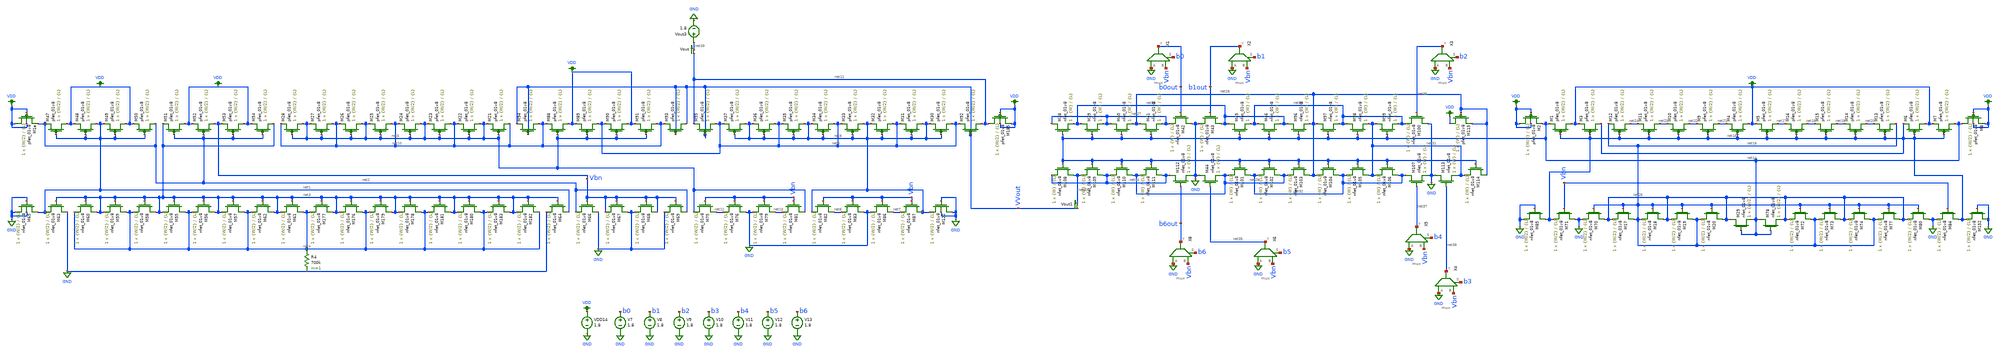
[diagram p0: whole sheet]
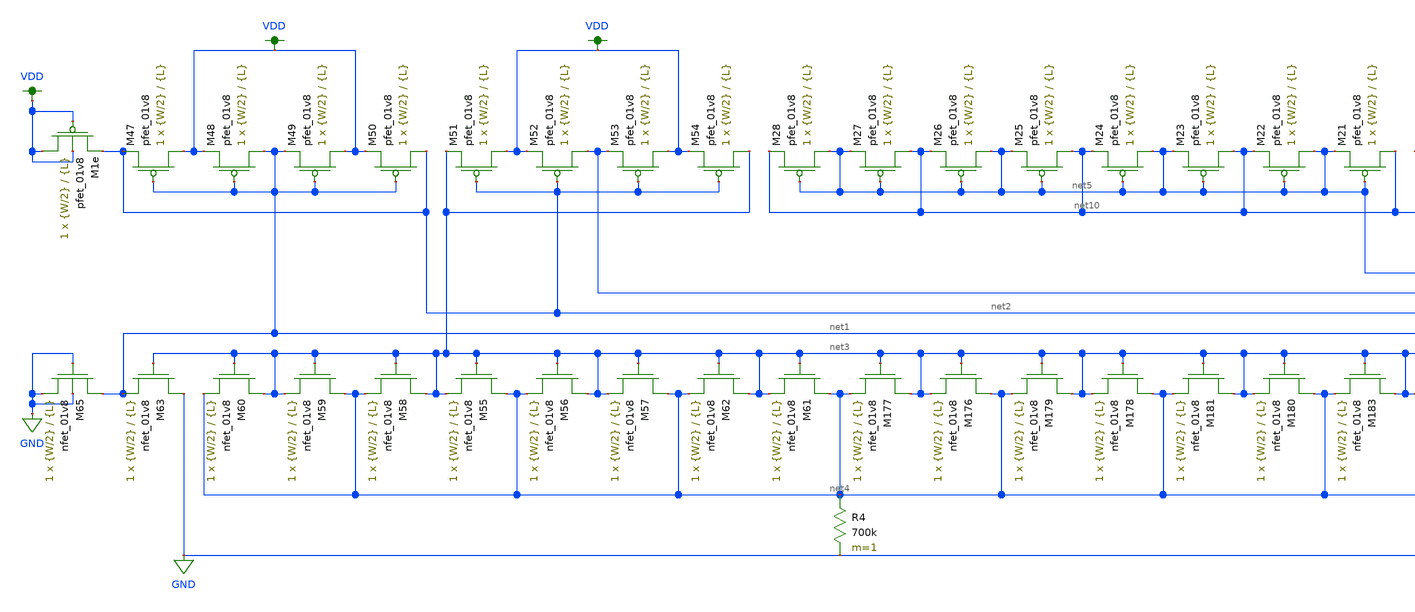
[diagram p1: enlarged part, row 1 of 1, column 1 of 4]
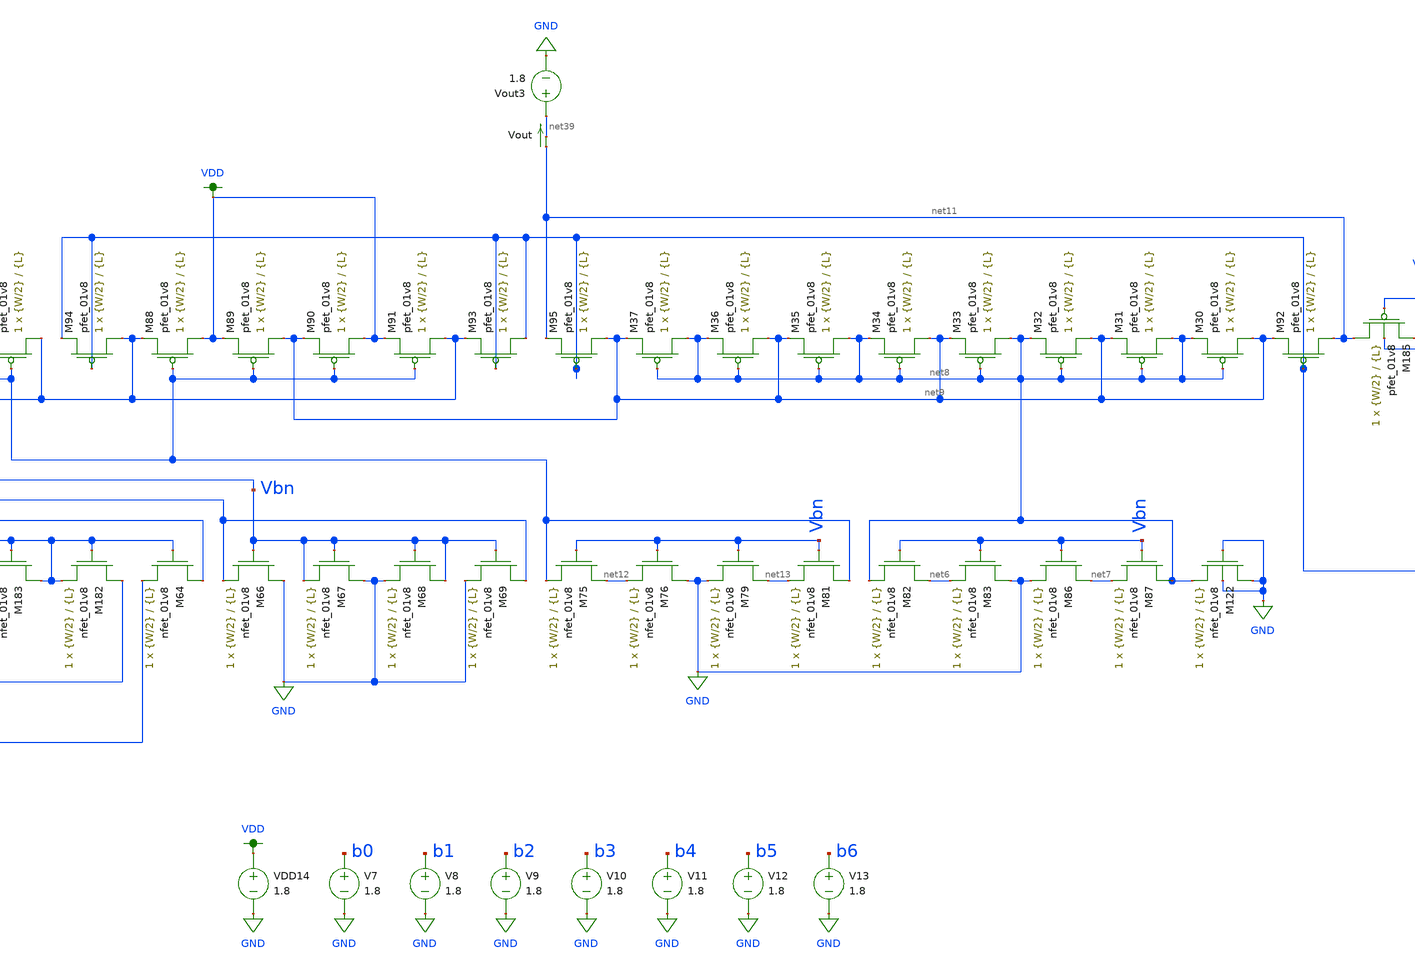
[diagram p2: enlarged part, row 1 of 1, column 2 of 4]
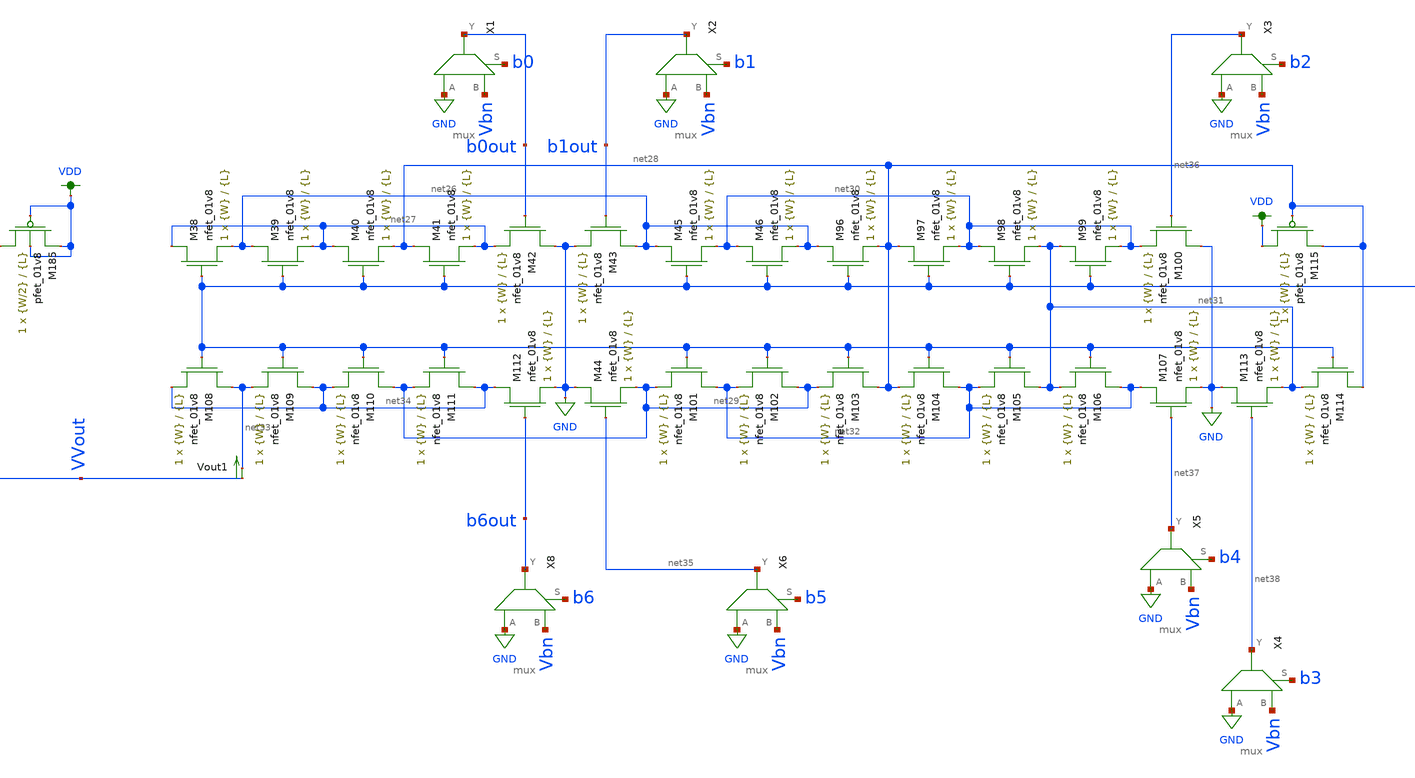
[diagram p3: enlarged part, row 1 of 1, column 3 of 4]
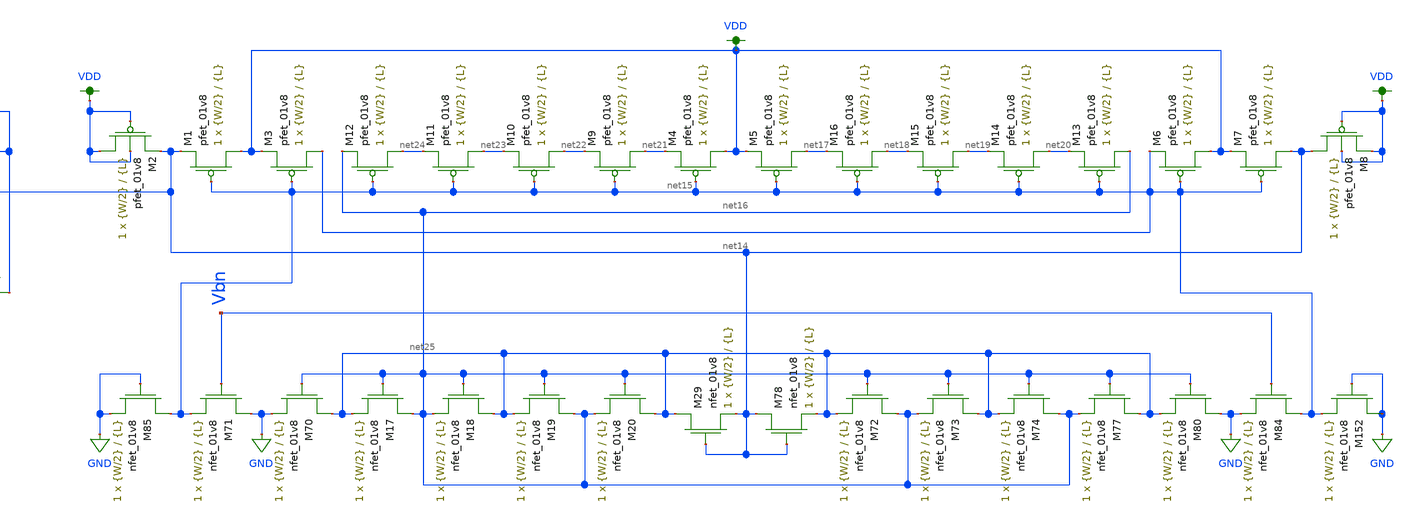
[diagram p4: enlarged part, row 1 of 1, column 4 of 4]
** sch_path: schematics/dac_voltage_current_current_mirror_lds.sch
**.subckt dac_voltage_current_current_mirror_lds
XM47 VDD net1 net2 VDD sky130_fd_pr__pfet_01v8 L={L} W={W/2} nf=1 ad='int((nf+1)/2) * W/nf * 0.29' as='int((nf+2)/2) * W/nf * 0.29'
+ pd='2*int((nf+1)/2) * (W/nf + 0.29)' ps='2*int((nf+2)/2) * (W/nf + 0.29)' nrd='0.29 / W' nrs='0.29 / W'
+ sa=0 sb=0 sd=0 mult=1 m=1
XM48 net1 net1 VDD VDD sky130_fd_pr__pfet_01v8 L={L} W={W/2} nf=1 ad='int((nf+1)/2) * W/nf * 0.29' as='int((nf+2)/2) * W/nf * 0.29'
+ pd='2*int((nf+1)/2) * (W/nf + 0.29)' ps='2*int((nf+2)/2) * (W/nf + 0.29)' nrd='0.29 / W' nrs='0.29 / W'
+ sa=0 sb=0 sd=0 mult=1 m=1
XM49 VDD net1 net1 VDD sky130_fd_pr__pfet_01v8 L={L} W={W/2} nf=1 ad='int((nf+1)/2) * W/nf * 0.29' as='int((nf+2)/2) * W/nf * 0.29'
+ pd='2*int((nf+1)/2) * (W/nf + 0.29)' ps='2*int((nf+2)/2) * (W/nf + 0.29)' nrd='0.29 / W' nrs='0.29 / W'
+ sa=0 sb=0 sd=0 mult=1 m=1
XM50 net2 net1 VDD VDD sky130_fd_pr__pfet_01v8 L={L} W={W/2} nf=1 ad='int((nf+1)/2) * W/nf * 0.29' as='int((nf+2)/2) * W/nf * 0.29'
+ pd='2*int((nf+1)/2) * (W/nf + 0.29)' ps='2*int((nf+2)/2) * (W/nf + 0.29)' nrd='0.29 / W' nrs='0.29 / W'
+ sa=0 sb=0 sd=0 mult=1 m=1
XM51 VDD net2 net3 VDD sky130_fd_pr__pfet_01v8 L={L} W={W/2} nf=1 ad='int((nf+1)/2) * W/nf * 0.29' as='int((nf+2)/2) * W/nf * 0.29'
+ pd='2*int((nf+1)/2) * (W/nf + 0.29)' ps='2*int((nf+2)/2) * (W/nf + 0.29)' nrd='0.29 / W' nrs='0.29 / W'
+ sa=0 sb=0 sd=0 mult=1 m=1
XM52 Vbn net2 VDD VDD sky130_fd_pr__pfet_01v8 L={L} W={W/2} nf=1 ad='int((nf+1)/2) * W/nf * 0.29' as='int((nf+2)/2) * W/nf * 0.29'
+ pd='2*int((nf+1)/2) * (W/nf + 0.29)' ps='2*int((nf+2)/2) * (W/nf + 0.29)' nrd='0.29 / W' nrs='0.29 / W'
+ sa=0 sb=0 sd=0 mult=1 m=1
XM53 VDD net2 Vbn VDD sky130_fd_pr__pfet_01v8 L={L} W={W/2} nf=1 ad='int((nf+1)/2) * W/nf * 0.29' as='int((nf+2)/2) * W/nf * 0.29'
+ pd='2*int((nf+1)/2) * (W/nf + 0.29)' ps='2*int((nf+2)/2) * (W/nf + 0.29)' nrd='0.29 / W' nrs='0.29 / W'
+ sa=0 sb=0 sd=0 mult=1 m=1
XM54 net3 net2 VDD VDD sky130_fd_pr__pfet_01v8 L={L} W={W/2} nf=1 ad='int((nf+1)/2) * W/nf * 0.29' as='int((nf+2)/2) * W/nf * 0.29'
+ pd='2*int((nf+1)/2) * (W/nf + 0.29)' ps='2*int((nf+2)/2) * (W/nf + 0.29)' nrd='0.29 / W' nrs='0.29 / W'
+ sa=0 sb=0 sd=0 mult=1 m=1
XM55 net4 net3 net3 GND sky130_fd_pr__nfet_01v8 L={L} W={W/2} nf=1 ad='int((nf+1)/2) * W/nf * 0.29' as='int((nf+2)/2) * W/nf * 0.29'
+ pd='2*int((nf+1)/2) * (W/nf + 0.29)' ps='2*int((nf+2)/2) * (W/nf + 0.29)' nrd='0.29 / W' nrs='0.29 / W'
+ sa=0 sb=0 sd=0 mult=1 m=1
XM56 net3 net3 net4 GND sky130_fd_pr__nfet_01v8 L={L} W={W/2} nf=1 ad='int((nf+1)/2) * W/nf * 0.29' as='int((nf+2)/2) * W/nf * 0.29'
+ pd='2*int((nf+1)/2) * (W/nf + 0.29)' ps='2*int((nf+2)/2) * (W/nf + 0.29)' nrd='0.29 / W' nrs='0.29 / W'
+ sa=0 sb=0 sd=0 mult=1 m=1
XM57 net4 net3 net3 GND sky130_fd_pr__nfet_01v8 L={L} W={W/2} nf=1 ad='int((nf+1)/2) * W/nf * 0.29' as='int((nf+2)/2) * W/nf * 0.29'
+ pd='2*int((nf+1)/2) * (W/nf + 0.29)' ps='2*int((nf+2)/2) * (W/nf + 0.29)' nrd='0.29 / W' nrs='0.29 / W'
+ sa=0 sb=0 sd=0 mult=1 m=1
XM58 net3 net3 net4 GND sky130_fd_pr__nfet_01v8 L={L} W={W/2} nf=1 ad='int((nf+1)/2) * W/nf * 0.29' as='int((nf+2)/2) * W/nf * 0.29'
+ pd='2*int((nf+1)/2) * (W/nf + 0.29)' ps='2*int((nf+2)/2) * (W/nf + 0.29)' nrd='0.29 / W' nrs='0.29 / W'
+ sa=0 sb=0 sd=0 mult=1 m=1
XM59 net4 net3 net3 GND sky130_fd_pr__nfet_01v8 L={L} W={W/2} nf=1 ad='int((nf+1)/2) * W/nf * 0.29' as='int((nf+2)/2) * W/nf * 0.29'
+ pd='2*int((nf+1)/2) * (W/nf + 0.29)' ps='2*int((nf+2)/2) * (W/nf + 0.29)' nrd='0.29 / W' nrs='0.29 / W'
+ sa=0 sb=0 sd=0 mult=1 m=1
XM60 net3 net3 net4 GND sky130_fd_pr__nfet_01v8 L={L} W={W/2} nf=1 ad='int((nf+1)/2) * W/nf * 0.29' as='int((nf+2)/2) * W/nf * 0.29'
+ pd='2*int((nf+1)/2) * (W/nf + 0.29)' ps='2*int((nf+2)/2) * (W/nf + 0.29)' nrd='0.29 / W' nrs='0.29 / W'
+ sa=0 sb=0 sd=0 mult=1 m=1
XM61 net4 net3 net3 GND sky130_fd_pr__nfet_01v8 L={L} W={W/2} nf=1 ad='int((nf+1)/2) * W/nf * 0.29' as='int((nf+2)/2) * W/nf * 0.29'
+ pd='2*int((nf+1)/2) * (W/nf + 0.29)' ps='2*int((nf+2)/2) * (W/nf + 0.29)' nrd='0.29 / W' nrs='0.29 / W'
+ sa=0 sb=0 sd=0 mult=1 m=1
XM62 net3 net3 net4 GND sky130_fd_pr__nfet_01v8 L={L} W={W/2} nf=1 ad='int((nf+1)/2) * W/nf * 0.29' as='int((nf+2)/2) * W/nf * 0.29'
+ pd='2*int((nf+1)/2) * (W/nf + 0.29)' ps='2*int((nf+2)/2) * (W/nf + 0.29)' nrd='0.29 / W' nrs='0.29 / W'
+ sa=0 sb=0 sd=0 mult=1 m=1
XM63 GND net3 net1 GND sky130_fd_pr__nfet_01v8 L={L} W={W/2} nf=1 ad='int((nf+1)/2) * W/nf * 0.29' as='int((nf+2)/2) * W/nf * 0.29'
+ pd='2*int((nf+1)/2) * (W/nf + 0.29)' ps='2*int((nf+2)/2) * (W/nf + 0.29)' nrd='0.29 / W' nrs='0.29 / W'
+ sa=0 sb=0 sd=0 mult=1 m=1
XM64 net1 net3 GND GND sky130_fd_pr__nfet_01v8 L={L} W={W/2} nf=1 ad='int((nf+1)/2) * W/nf * 0.29' as='int((nf+2)/2) * W/nf * 0.29'
+ pd='2*int((nf+1)/2) * (W/nf + 0.29)' ps='2*int((nf+2)/2) * (W/nf + 0.29)' nrd='0.29 / W' nrs='0.29 / W'
+ sa=0 sb=0 sd=0 mult=1 m=1
R4 net4 GND 700k m=1
XM1e VDD VDD net2 VDD sky130_fd_pr__pfet_01v8 L={L} W={W/2} nf=1 ad='int((nf+1)/2) * W/nf * 0.29' as='int((nf+2)/2) * W/nf * 0.29'
+ pd='2*int((nf+1)/2) * (W/nf + 0.29)' ps='2*int((nf+2)/2) * (W/nf + 0.29)' nrd='0.29 / W' nrs='0.29 / W'
+ sa=0 sb=0 sd=0 mult=1 m=1
XM65 net1 GND GND GND sky130_fd_pr__nfet_01v8 L={L} W={W/2} nf=1 ad='int((nf+1)/2) * W/nf * 0.29' as='int((nf+2)/2) * W/nf * 0.29'
+ pd='2*int((nf+1)/2) * (W/nf + 0.29)' ps='2*int((nf+2)/2) * (W/nf + 0.29)' nrd='0.29 / W' nrs='0.29 / W'
+ sa=0 sb=0 sd=0 mult=1 m=1
XM66 GND Vbn net2 GND sky130_fd_pr__nfet_01v8 L={L} W={W/2} nf=1 ad='int((nf+1)/2) * W/nf * 0.29' as='int((nf+2)/2) * W/nf * 0.29'
+ pd='2*int((nf+1)/2) * (W/nf + 0.29)' ps='2*int((nf+2)/2) * (W/nf + 0.29)' nrd='0.29 / W' nrs='0.29 / W'
+ sa=0 sb=0 sd=0 mult=1 m=1
XM67 GND Vbn Vbn GND sky130_fd_pr__nfet_01v8 L={L} W={W/2} nf=1 ad='int((nf+1)/2) * W/nf * 0.29' as='int((nf+2)/2) * W/nf * 0.29'
+ pd='2*int((nf+1)/2) * (W/nf + 0.29)' ps='2*int((nf+2)/2) * (W/nf + 0.29)' nrd='0.29 / W' nrs='0.29 / W'
+ sa=0 sb=0 sd=0 mult=1 m=1
XM68 Vbn Vbn GND GND sky130_fd_pr__nfet_01v8 L={L} W={W/2} nf=1 ad='int((nf+1)/2) * W/nf * 0.29' as='int((nf+2)/2) * W/nf * 0.29'
+ pd='2*int((nf+1)/2) * (W/nf + 0.29)' ps='2*int((nf+2)/2) * (W/nf + 0.29)' nrd='0.29 / W' nrs='0.29 / W'
+ sa=0 sb=0 sd=0 mult=1 m=1
XM69 net2 Vbn GND GND sky130_fd_pr__nfet_01v8 L={L} W={W/2} nf=1 ad='int((nf+1)/2) * W/nf * 0.29' as='int((nf+2)/2) * W/nf * 0.29'
+ pd='2*int((nf+1)/2) * (W/nf + 0.29)' ps='2*int((nf+2)/2) * (W/nf + 0.29)' nrd='0.29 / W' nrs='0.29 / W'
+ sa=0 sb=0 sd=0 mult=1 m=1
XM75 net12 Vbn net5 GND sky130_fd_pr__nfet_01v8 L={L} W={W/2} nf=1 ad='int((nf+1)/2) * W/nf * 0.29' as='int((nf+2)/2) * W/nf * 0.29'
+ pd='2*int((nf+1)/2) * (W/nf + 0.29)' ps='2*int((nf+2)/2) * (W/nf + 0.29)' nrd='0.29 / W' nrs='0.29 / W'
+ sa=0 sb=0 sd=0 mult=1 m=1
XM76 GND Vbn net12 GND sky130_fd_pr__nfet_01v8 L={L} W={W/2} nf=1 ad='int((nf+1)/2) * W/nf * 0.29' as='int((nf+2)/2) * W/nf * 0.29'
+ pd='2*int((nf+1)/2) * (W/nf + 0.29)' ps='2*int((nf+2)/2) * (W/nf + 0.29)' nrd='0.29 / W' nrs='0.29 / W'
+ sa=0 sb=0 sd=0 mult=1 m=1
XM79 net13 Vbn GND GND sky130_fd_pr__nfet_01v8 L={L} W={W/2} nf=1 ad='int((nf+1)/2) * W/nf * 0.29' as='int((nf+2)/2) * W/nf * 0.29'
+ pd='2*int((nf+1)/2) * (W/nf + 0.29)' ps='2*int((nf+2)/2) * (W/nf + 0.29)' nrd='0.29 / W' nrs='0.29 / W'
+ sa=0 sb=0 sd=0 mult=1 m=1
XM81 net5 Vbn net13 GND sky130_fd_pr__nfet_01v8 L={L} W={W/2} nf=1 ad='int((nf+1)/2) * W/nf * 0.29' as='int((nf+2)/2) * W/nf * 0.29'
+ pd='2*int((nf+1)/2) * (W/nf + 0.29)' ps='2*int((nf+2)/2) * (W/nf + 0.29)' nrd='0.29 / W' nrs='0.29 / W'
+ sa=0 sb=0 sd=0 mult=1 m=1
XM82 net6 Vbn net8 GND sky130_fd_pr__nfet_01v8 L={L} W={W/2} nf=1 ad='int((nf+1)/2) * W/nf * 0.29' as='int((nf+2)/2) * W/nf * 0.29'
+ pd='2*int((nf+1)/2) * (W/nf + 0.29)' ps='2*int((nf+2)/2) * (W/nf + 0.29)' nrd='0.29 / W' nrs='0.29 / W'
+ sa=0 sb=0 sd=0 mult=1 m=1
XM83 GND Vbn net6 GND sky130_fd_pr__nfet_01v8 L={L} W={W/2} nf=1 ad='int((nf+1)/2) * W/nf * 0.29' as='int((nf+2)/2) * W/nf * 0.29'
+ pd='2*int((nf+1)/2) * (W/nf + 0.29)' ps='2*int((nf+2)/2) * (W/nf + 0.29)' nrd='0.29 / W' nrs='0.29 / W'
+ sa=0 sb=0 sd=0 mult=1 m=1
XM86 net7 Vbn GND GND sky130_fd_pr__nfet_01v8 L={L} W={W/2} nf=1 ad='int((nf+1)/2) * W/nf * 0.29' as='int((nf+2)/2) * W/nf * 0.29'
+ pd='2*int((nf+1)/2) * (W/nf + 0.29)' ps='2*int((nf+2)/2) * (W/nf + 0.29)' nrd='0.29 / W' nrs='0.29 / W'
+ sa=0 sb=0 sd=0 mult=1 m=1
XM87 net8 Vbn net7 GND sky130_fd_pr__nfet_01v8 L={L} W={W/2} nf=1 ad='int((nf+1)/2) * W/nf * 0.29' as='int((nf+2)/2) * W/nf * 0.29'
+ pd='2*int((nf+1)/2) * (W/nf + 0.29)' ps='2*int((nf+2)/2) * (W/nf + 0.29)' nrd='0.29 / W' nrs='0.29 / W'
+ sa=0 sb=0 sd=0 mult=1 m=1
XM88 VDD net5 net10 VDD sky130_fd_pr__pfet_01v8 L={L} W={W/2} nf=1 ad='int((nf+1)/2) * W/nf * 0.29' as='int((nf+2)/2) * W/nf * 0.29'
+ pd='2*int((nf+1)/2) * (W/nf + 0.29)' ps='2*int((nf+2)/2) * (W/nf + 0.29)' nrd='0.29 / W' nrs='0.29 / W'
+ sa=0 sb=0 sd=0 mult=1 m=1
XM89 net9 net5 VDD VDD sky130_fd_pr__pfet_01v8 L={L} W={W/2} nf=1 ad='int((nf+1)/2) * W/nf * 0.29' as='int((nf+2)/2) * W/nf * 0.29'
+ pd='2*int((nf+1)/2) * (W/nf + 0.29)' ps='2*int((nf+2)/2) * (W/nf + 0.29)' nrd='0.29 / W' nrs='0.29 / W'
+ sa=0 sb=0 sd=0 mult=1 m=1
XM90 VDD net5 net9 VDD sky130_fd_pr__pfet_01v8 L={L} W={W/2} nf=1 ad='int((nf+1)/2) * W/nf * 0.29' as='int((nf+2)/2) * W/nf * 0.29'
+ pd='2*int((nf+1)/2) * (W/nf + 0.29)' ps='2*int((nf+2)/2) * (W/nf + 0.29)' nrd='0.29 / W' nrs='0.29 / W'
+ sa=0 sb=0 sd=0 mult=1 m=1
XM91 net10 net5 VDD VDD sky130_fd_pr__pfet_01v8 L={L} W={W/2} nf=1 ad='int((nf+1)/2) * W/nf * 0.29' as='int((nf+2)/2) * W/nf * 0.29'
+ pd='2*int((nf+1)/2) * (W/nf + 0.29)' ps='2*int((nf+2)/2) * (W/nf + 0.29)' nrd='0.29 / W' nrs='0.29 / W'
+ sa=0 sb=0 sd=0 mult=1 m=1
XM92 net11 VVout net9 VDD sky130_fd_pr__pfet_01v8 L={L} W={W/2} nf=1 ad='int((nf+1)/2) * W/nf * 0.29'
+ as='int((nf+2)/2) * W/nf * 0.29' pd='2*int((nf+1)/2) * (W/nf + 0.29)' ps='2*int((nf+2)/2) * (W/nf + 0.29)'
+ nrd='0.29 / W' nrs='0.29 / W' sa=0 sb=0 sd=0 mult=1 m=1
XM93 VVout VVout net10 VDD sky130_fd_pr__pfet_01v8 L={L} W={W/2} nf=1 ad='int((nf+1)/2) * W/nf * 0.29'
+ as='int((nf+2)/2) * W/nf * 0.29' pd='2*int((nf+1)/2) * (W/nf + 0.29)' ps='2*int((nf+2)/2) * (W/nf + 0.29)'
+ nrd='0.29 / W' nrs='0.29 / W' sa=0 sb=0 sd=0 mult=1 m=1
XM94 net10 VVout VVout VDD sky130_fd_pr__pfet_01v8 L={L} W={W/2} nf=1 ad='int((nf+1)/2) * W/nf * 0.29'
+ as='int((nf+2)/2) * W/nf * 0.29' pd='2*int((nf+1)/2) * (W/nf + 0.29)' ps='2*int((nf+2)/2) * (W/nf + 0.29)'
+ nrd='0.29 / W' nrs='0.29 / W' sa=0 sb=0 sd=0 mult=1 m=1
XM95 net9 VVout net11 VDD sky130_fd_pr__pfet_01v8 L={L} W={W/2} nf=1 ad='int((nf+1)/2) * W/nf * 0.29'
+ as='int((nf+2)/2) * W/nf * 0.29' pd='2*int((nf+1)/2) * (W/nf + 0.29)' ps='2*int((nf+2)/2) * (W/nf + 0.29)'
+ nrd='0.29 / W' nrs='0.29 / W' sa=0 sb=0 sd=0 mult=1 m=1
XM176 net4 net3 net3 GND sky130_fd_pr__nfet_01v8 L={L} W={W/2} nf=1 ad='int((nf+1)/2) * W/nf * 0.29'
+ as='int((nf+2)/2) * W/nf * 0.29' pd='2*int((nf+1)/2) * (W/nf + 0.29)' ps='2*int((nf+2)/2) * (W/nf + 0.29)'
+ nrd='0.29 / W' nrs='0.29 / W' sa=0 sb=0 sd=0 mult=1 m=1
XM177 net3 net3 net4 GND sky130_fd_pr__nfet_01v8 L={L} W={W/2} nf=1 ad='int((nf+1)/2) * W/nf * 0.29'
+ as='int((nf+2)/2) * W/nf * 0.29' pd='2*int((nf+1)/2) * (W/nf + 0.29)' ps='2*int((nf+2)/2) * (W/nf + 0.29)'
+ nrd='0.29 / W' nrs='0.29 / W' sa=0 sb=0 sd=0 mult=1 m=1
XM178 net4 net3 net3 GND sky130_fd_pr__nfet_01v8 L={L} W={W/2} nf=1 ad='int((nf+1)/2) * W/nf * 0.29'
+ as='int((nf+2)/2) * W/nf * 0.29' pd='2*int((nf+1)/2) * (W/nf + 0.29)' ps='2*int((nf+2)/2) * (W/nf + 0.29)'
+ nrd='0.29 / W' nrs='0.29 / W' sa=0 sb=0 sd=0 mult=1 m=1
XM179 net3 net3 net4 GND sky130_fd_pr__nfet_01v8 L={L} W={W/2} nf=1 ad='int((nf+1)/2) * W/nf * 0.29'
+ as='int((nf+2)/2) * W/nf * 0.29' pd='2*int((nf+1)/2) * (W/nf + 0.29)' ps='2*int((nf+2)/2) * (W/nf + 0.29)'
+ nrd='0.29 / W' nrs='0.29 / W' sa=0 sb=0 sd=0 mult=1 m=1
XM180 net4 net3 net3 GND sky130_fd_pr__nfet_01v8 L={L} W={W/2} nf=1 ad='int((nf+1)/2) * W/nf * 0.29'
+ as='int((nf+2)/2) * W/nf * 0.29' pd='2*int((nf+1)/2) * (W/nf + 0.29)' ps='2*int((nf+2)/2) * (W/nf + 0.29)'
+ nrd='0.29 / W' nrs='0.29 / W' sa=0 sb=0 sd=0 mult=1 m=1
XM181 net3 net3 net4 GND sky130_fd_pr__nfet_01v8 L={L} W={W/2} nf=1 ad='int((nf+1)/2) * W/nf * 0.29'
+ as='int((nf+2)/2) * W/nf * 0.29' pd='2*int((nf+1)/2) * (W/nf + 0.29)' ps='2*int((nf+2)/2) * (W/nf + 0.29)'
+ nrd='0.29 / W' nrs='0.29 / W' sa=0 sb=0 sd=0 mult=1 m=1
XM182 net4 net3 net3 GND sky130_fd_pr__nfet_01v8 L={L} W={W/2} nf=1 ad='int((nf+1)/2) * W/nf * 0.29'
+ as='int((nf+2)/2) * W/nf * 0.29' pd='2*int((nf+1)/2) * (W/nf + 0.29)' ps='2*int((nf+2)/2) * (W/nf + 0.29)'
+ nrd='0.29 / W' nrs='0.29 / W' sa=0 sb=0 sd=0 mult=1 m=1
XM183 net3 net3 net4 GND sky130_fd_pr__nfet_01v8 L={L} W={W/2} nf=1 ad='int((nf+1)/2) * W/nf * 0.29'
+ as='int((nf+2)/2) * W/nf * 0.29' pd='2*int((nf+1)/2) * (W/nf + 0.29)' ps='2*int((nf+2)/2) * (W/nf + 0.29)'
+ nrd='0.29 / W' nrs='0.29 / W' sa=0 sb=0 sd=0 mult=1 m=1
XM185 net11 VDD VDD VDD sky130_fd_pr__pfet_01v8 L={L} W={W/2} nf=1 ad='int((nf+1)/2) * W/nf * 0.29' as='int((nf+2)/2) * W/nf * 0.29'
+ pd='2*int((nf+1)/2) * (W/nf + 0.29)' ps='2*int((nf+2)/2) * (W/nf + 0.29)' nrd='0.29 / W' nrs='0.29 / W'
+ sa=0 sb=0 sd=0 mult=1 m=1
Vout net11 net39 0
.save i(vout)
XM21 net10 net5 net5 VDD sky130_fd_pr__pfet_01v8 L={L} W={W/2} nf=1 ad='int((nf+1)/2) * W/nf * 0.29'
+ as='int((nf+2)/2) * W/nf * 0.29' pd='2*int((nf+1)/2) * (W/nf + 0.29)' ps='2*int((nf+2)/2) * (W/nf + 0.29)'
+ nrd='0.29 / W' nrs='0.29 / W' sa=0 sb=0 sd=0 mult=1 m=1
XM22 net5 net5 net10 VDD sky130_fd_pr__pfet_01v8 L={L} W={W/2} nf=1 ad='int((nf+1)/2) * W/nf * 0.29'
+ as='int((nf+2)/2) * W/nf * 0.29' pd='2*int((nf+1)/2) * (W/nf + 0.29)' ps='2*int((nf+2)/2) * (W/nf + 0.29)'
+ nrd='0.29 / W' nrs='0.29 / W' sa=0 sb=0 sd=0 mult=1 m=1
XM23 net10 net5 net5 VDD sky130_fd_pr__pfet_01v8 L={L} W={W/2} nf=1 ad='int((nf+1)/2) * W/nf * 0.29'
+ as='int((nf+2)/2) * W/nf * 0.29' pd='2*int((nf+1)/2) * (W/nf + 0.29)' ps='2*int((nf+2)/2) * (W/nf + 0.29)'
+ nrd='0.29 / W' nrs='0.29 / W' sa=0 sb=0 sd=0 mult=1 m=1
XM24 net5 net5 net10 VDD sky130_fd_pr__pfet_01v8 L={L} W={W/2} nf=1 ad='int((nf+1)/2) * W/nf * 0.29'
+ as='int((nf+2)/2) * W/nf * 0.29' pd='2*int((nf+1)/2) * (W/nf + 0.29)' ps='2*int((nf+2)/2) * (W/nf + 0.29)'
+ nrd='0.29 / W' nrs='0.29 / W' sa=0 sb=0 sd=0 mult=1 m=1
XM25 net10 net5 net5 VDD sky130_fd_pr__pfet_01v8 L={L} W={W/2} nf=1 ad='int((nf+1)/2) * W/nf * 0.29'
+ as='int((nf+2)/2) * W/nf * 0.29' pd='2*int((nf+1)/2) * (W/nf + 0.29)' ps='2*int((nf+2)/2) * (W/nf + 0.29)'
+ nrd='0.29 / W' nrs='0.29 / W' sa=0 sb=0 sd=0 mult=1 m=1
XM26 net5 net5 net10 VDD sky130_fd_pr__pfet_01v8 L={L} W={W/2} nf=1 ad='int((nf+1)/2) * W/nf * 0.29'
+ as='int((nf+2)/2) * W/nf * 0.29' pd='2*int((nf+1)/2) * (W/nf + 0.29)' ps='2*int((nf+2)/2) * (W/nf + 0.29)'
+ nrd='0.29 / W' nrs='0.29 / W' sa=0 sb=0 sd=0 mult=1 m=1
XM27 net10 net5 net5 VDD sky130_fd_pr__pfet_01v8 L={L} W={W/2} nf=1 ad='int((nf+1)/2) * W/nf * 0.29'
+ as='int((nf+2)/2) * W/nf * 0.29' pd='2*int((nf+1)/2) * (W/nf + 0.29)' ps='2*int((nf+2)/2) * (W/nf + 0.29)'
+ nrd='0.29 / W' nrs='0.29 / W' sa=0 sb=0 sd=0 mult=1 m=1
XM28 net5 net5 net10 VDD sky130_fd_pr__pfet_01v8 L={L} W={W/2} nf=1 ad='int((nf+1)/2) * W/nf * 0.29'
+ as='int((nf+2)/2) * W/nf * 0.29' pd='2*int((nf+1)/2) * (W/nf + 0.29)' ps='2*int((nf+2)/2) * (W/nf + 0.29)'
+ nrd='0.29 / W' nrs='0.29 / W' sa=0 sb=0 sd=0 mult=1 m=1
XM30 net9 net8 net8 VDD sky130_fd_pr__pfet_01v8 L={L} W={W/2} nf=1 ad='int((nf+1)/2) * W/nf * 0.29' as='int((nf+2)/2) * W/nf * 0.29'
+ pd='2*int((nf+1)/2) * (W/nf + 0.29)' ps='2*int((nf+2)/2) * (W/nf + 0.29)' nrd='0.29 / W' nrs='0.29 / W'
+ sa=0 sb=0 sd=0 mult=1 m=1
XM31 net8 net8 net9 VDD sky130_fd_pr__pfet_01v8 L={L} W={W/2} nf=1 ad='int((nf+1)/2) * W/nf * 0.29' as='int((nf+2)/2) * W/nf * 0.29'
+ pd='2*int((nf+1)/2) * (W/nf + 0.29)' ps='2*int((nf+2)/2) * (W/nf + 0.29)' nrd='0.29 / W' nrs='0.29 / W'
+ sa=0 sb=0 sd=0 mult=1 m=1
XM32 net9 net8 net8 VDD sky130_fd_pr__pfet_01v8 L={L} W={W/2} nf=1 ad='int((nf+1)/2) * W/nf * 0.29' as='int((nf+2)/2) * W/nf * 0.29'
+ pd='2*int((nf+1)/2) * (W/nf + 0.29)' ps='2*int((nf+2)/2) * (W/nf + 0.29)' nrd='0.29 / W' nrs='0.29 / W'
+ sa=0 sb=0 sd=0 mult=1 m=1
XM33 net8 net8 net9 VDD sky130_fd_pr__pfet_01v8 L={L} W={W/2} nf=1 ad='int((nf+1)/2) * W/nf * 0.29' as='int((nf+2)/2) * W/nf * 0.29'
+ pd='2*int((nf+1)/2) * (W/nf + 0.29)' ps='2*int((nf+2)/2) * (W/nf + 0.29)' nrd='0.29 / W' nrs='0.29 / W'
+ sa=0 sb=0 sd=0 mult=1 m=1
XM34 net9 net8 net8 VDD sky130_fd_pr__pfet_01v8 L={L} W={W/2} nf=1 ad='int((nf+1)/2) * W/nf * 0.29' as='int((nf+2)/2) * W/nf * 0.29'
+ pd='2*int((nf+1)/2) * (W/nf + 0.29)' ps='2*int((nf+2)/2) * (W/nf + 0.29)' nrd='0.29 / W' nrs='0.29 / W'
+ sa=0 sb=0 sd=0 mult=1 m=1
XM35 net8 net8 net9 VDD sky130_fd_pr__pfet_01v8 L={L} W={W/2} nf=1 ad='int((nf+1)/2) * W/nf * 0.29' as='int((nf+2)/2) * W/nf * 0.29'
+ pd='2*int((nf+1)/2) * (W/nf + 0.29)' ps='2*int((nf+2)/2) * (W/nf + 0.29)' nrd='0.29 / W' nrs='0.29 / W'
+ sa=0 sb=0 sd=0 mult=1 m=1
XM36 net9 net8 net8 VDD sky130_fd_pr__pfet_01v8 L={L} W={W/2} nf=1 ad='int((nf+1)/2) * W/nf * 0.29' as='int((nf+2)/2) * W/nf * 0.29'
+ pd='2*int((nf+1)/2) * (W/nf + 0.29)' ps='2*int((nf+2)/2) * (W/nf + 0.29)' nrd='0.29 / W' nrs='0.29 / W'
+ sa=0 sb=0 sd=0 mult=1 m=1
XM37 net8 net8 net9 VDD sky130_fd_pr__pfet_01v8 L={L} W={W/2} nf=1 ad='int((nf+1)/2) * W/nf * 0.29' as='int((nf+2)/2) * W/nf * 0.29'
+ pd='2*int((nf+1)/2) * (W/nf + 0.29)' ps='2*int((nf+2)/2) * (W/nf + 0.29)' nrd='0.29 / W' nrs='0.29 / W'
+ sa=0 sb=0 sd=0 mult=1 m=1
XM122 GND GND net8 GND sky130_fd_pr__nfet_01v8 L={L} W={W/2} nf=1 ad='int((nf+1)/2) * W/nf * 0.29' as='int((nf+2)/2) * W/nf * 0.29'
+ pd='2*int((nf+1)/2) * (W/nf + 0.29)' ps='2*int((nf+2)/2) * (W/nf + 0.29)' nrd='0.29 / W' nrs='0.29 / W'
+ sa=0 sb=0 sd=0 mult=1 m=1
XM1 VDD net15 net14 VDD sky130_fd_pr__pfet_01v8 L={L} W={W/2} nf=1 ad='int((nf+1)/2) * W/nf * 0.29' as='int((nf+2)/2) * W/nf * 0.29'
+ pd='2*int((nf+1)/2) * (W/nf + 0.29)' ps='2*int((nf+2)/2) * (W/nf + 0.29)' nrd='0.29 / W' nrs='0.29 / W'
+ sa=0 sb=0 sd=0 mult=1 m=1
XM2 VDD VDD net14 VDD sky130_fd_pr__pfet_01v8 L={L} W={W/2} nf=1 ad='int((nf+1)/2) * W/nf * 0.29' as='int((nf+2)/2) * W/nf * 0.29'
+ pd='2*int((nf+1)/2) * (W/nf + 0.29)' ps='2*int((nf+2)/2) * (W/nf + 0.29)' nrd='0.29 / W' nrs='0.29 / W'
+ sa=0 sb=0 sd=0 mult=1 m=1
XM3 net15 net15 VDD VDD sky130_fd_pr__pfet_01v8 L={L} W={W/2} nf=1 ad='int((nf+1)/2) * W/nf * 0.29' as='int((nf+2)/2) * W/nf * 0.29'
+ pd='2*int((nf+1)/2) * (W/nf + 0.29)' ps='2*int((nf+2)/2) * (W/nf + 0.29)' nrd='0.29 / W' nrs='0.29 / W'
+ sa=0 sb=0 sd=0 mult=1 m=1
XM4 VDD net15 net21 VDD sky130_fd_pr__pfet_01v8 L={L} W={W/2} nf=1 ad='int((nf+1)/2) * W/nf * 0.29' as='int((nf+2)/2) * W/nf * 0.29'
+ pd='2*int((nf+1)/2) * (W/nf + 0.29)' ps='2*int((nf+2)/2) * (W/nf + 0.29)' nrd='0.29 / W' nrs='0.29 / W'
+ sa=0 sb=0 sd=0 mult=1 m=1
XM5 net17 net15 VDD VDD sky130_fd_pr__pfet_01v8 L={L} W={W/2} nf=1 ad='int((nf+1)/2) * W/nf * 0.29' as='int((nf+2)/2) * W/nf * 0.29'
+ pd='2*int((nf+1)/2) * (W/nf + 0.29)' ps='2*int((nf+2)/2) * (W/nf + 0.29)' nrd='0.29 / W' nrs='0.29 / W'
+ sa=0 sb=0 sd=0 mult=1 m=1
XM6 VDD net15 net15 VDD sky130_fd_pr__pfet_01v8 L={L} W={W/2} nf=1 ad='int((nf+1)/2) * W/nf * 0.29' as='int((nf+2)/2) * W/nf * 0.29'
+ pd='2*int((nf+1)/2) * (W/nf + 0.29)' ps='2*int((nf+2)/2) * (W/nf + 0.29)' nrd='0.29 / W' nrs='0.29 / W'
+ sa=0 sb=0 sd=0 mult=1 m=1
XM7 net14 net15 VDD VDD sky130_fd_pr__pfet_01v8 L={L} W={W/2} nf=1 ad='int((nf+1)/2) * W/nf * 0.29' as='int((nf+2)/2) * W/nf * 0.29'
+ pd='2*int((nf+1)/2) * (W/nf + 0.29)' ps='2*int((nf+2)/2) * (W/nf + 0.29)' nrd='0.29 / W' nrs='0.29 / W'
+ sa=0 sb=0 sd=0 mult=1 m=1
XM8 net14 VDD VDD VDD sky130_fd_pr__pfet_01v8 L={L} W={W/2} nf=1 ad='int((nf+1)/2) * W/nf * 0.29' as='int((nf+2)/2) * W/nf * 0.29'
+ pd='2*int((nf+1)/2) * (W/nf + 0.29)' ps='2*int((nf+2)/2) * (W/nf + 0.29)' nrd='0.29 / W' nrs='0.29 / W'
+ sa=0 sb=0 sd=0 mult=1 m=1
XM9 net21 net15 net22 VDD sky130_fd_pr__pfet_01v8 L={L} W={W/2} nf=1 ad='int((nf+1)/2) * W/nf * 0.29'
+ as='int((nf+2)/2) * W/nf * 0.29' pd='2*int((nf+1)/2) * (W/nf + 0.29)' ps='2*int((nf+2)/2) * (W/nf + 0.29)'
+ nrd='0.29 / W' nrs='0.29 / W' sa=0 sb=0 sd=0 mult=1 m=1
XM10 net22 net15 net23 VDD sky130_fd_pr__pfet_01v8 L={L} W={W/2} nf=1 ad='int((nf+1)/2) * W/nf * 0.29'
+ as='int((nf+2)/2) * W/nf * 0.29' pd='2*int((nf+1)/2) * (W/nf + 0.29)' ps='2*int((nf+2)/2) * (W/nf + 0.29)'
+ nrd='0.29 / W' nrs='0.29 / W' sa=0 sb=0 sd=0 mult=1 m=1
XM11 net23 net15 net24 VDD sky130_fd_pr__pfet_01v8 L={L} W={W/2} nf=1 ad='int((nf+1)/2) * W/nf * 0.29'
+ as='int((nf+2)/2) * W/nf * 0.29' pd='2*int((nf+1)/2) * (W/nf + 0.29)' ps='2*int((nf+2)/2) * (W/nf + 0.29)'
+ nrd='0.29 / W' nrs='0.29 / W' sa=0 sb=0 sd=0 mult=1 m=1
XM12 net24 net15 net16 VDD sky130_fd_pr__pfet_01v8 L={L} W={W/2} nf=1 ad='int((nf+1)/2) * W/nf * 0.29'
+ as='int((nf+2)/2) * W/nf * 0.29' pd='2*int((nf+1)/2) * (W/nf + 0.29)' ps='2*int((nf+2)/2) * (W/nf + 0.29)'
+ nrd='0.29 / W' nrs='0.29 / W' sa=0 sb=0 sd=0 mult=1 m=1
XM13 net16 net15 net20 VDD sky130_fd_pr__pfet_01v8 L={L} W={W/2} nf=1 ad='int((nf+1)/2) * W/nf * 0.29'
+ as='int((nf+2)/2) * W/nf * 0.29' pd='2*int((nf+1)/2) * (W/nf + 0.29)' ps='2*int((nf+2)/2) * (W/nf + 0.29)'
+ nrd='0.29 / W' nrs='0.29 / W' sa=0 sb=0 sd=0 mult=1 m=1
XM14 net20 net15 net19 VDD sky130_fd_pr__pfet_01v8 L={L} W={W/2} nf=1 ad='int((nf+1)/2) * W/nf * 0.29'
+ as='int((nf+2)/2) * W/nf * 0.29' pd='2*int((nf+1)/2) * (W/nf + 0.29)' ps='2*int((nf+2)/2) * (W/nf + 0.29)'
+ nrd='0.29 / W' nrs='0.29 / W' sa=0 sb=0 sd=0 mult=1 m=1
XM15 net19 net15 net18 VDD sky130_fd_pr__pfet_01v8 L={L} W={W/2} nf=1 ad='int((nf+1)/2) * W/nf * 0.29'
+ as='int((nf+2)/2) * W/nf * 0.29' pd='2*int((nf+1)/2) * (W/nf + 0.29)' ps='2*int((nf+2)/2) * (W/nf + 0.29)'
+ nrd='0.29 / W' nrs='0.29 / W' sa=0 sb=0 sd=0 mult=1 m=1
XM16 net18 net15 net17 VDD sky130_fd_pr__pfet_01v8 L={L} W={W/2} nf=1 ad='int((nf+1)/2) * W/nf * 0.29'
+ as='int((nf+2)/2) * W/nf * 0.29' pd='2*int((nf+1)/2) * (W/nf + 0.29)' ps='2*int((nf+2)/2) * (W/nf + 0.29)'
+ nrd='0.29 / W' nrs='0.29 / W' sa=0 sb=0 sd=0 mult=1 m=1
XM17 net16 net16 net25 GND sky130_fd_pr__nfet_01v8 L={L} W={W/2} nf=1 ad='int((nf+1)/2) * W/nf * 0.29'
+ as='int((nf+2)/2) * W/nf * 0.29' pd='2*int((nf+1)/2) * (W/nf + 0.29)' ps='2*int((nf+2)/2) * (W/nf + 0.29)'
+ nrd='0.29 / W' nrs='0.29 / W' sa=0 sb=0 sd=0 mult=1 m=1
XM18 net25 net16 net16 GND sky130_fd_pr__nfet_01v8 L={L} W={W/2} nf=1 ad='int((nf+1)/2) * W/nf * 0.29'
+ as='int((nf+2)/2) * W/nf * 0.29' pd='2*int((nf+1)/2) * (W/nf + 0.29)' ps='2*int((nf+2)/2) * (W/nf + 0.29)'
+ nrd='0.29 / W' nrs='0.29 / W' sa=0 sb=0 sd=0 mult=1 m=1
XM19 net16 net16 net25 GND sky130_fd_pr__nfet_01v8 L={L} W={W/2} nf=1 ad='int((nf+1)/2) * W/nf * 0.29'
+ as='int((nf+2)/2) * W/nf * 0.29' pd='2*int((nf+1)/2) * (W/nf + 0.29)' ps='2*int((nf+2)/2) * (W/nf + 0.29)'
+ nrd='0.29 / W' nrs='0.29 / W' sa=0 sb=0 sd=0 mult=1 m=1
XM20 net25 net16 net16 GND sky130_fd_pr__nfet_01v8 L={L} W={W/2} nf=1 ad='int((nf+1)/2) * W/nf * 0.29'
+ as='int((nf+2)/2) * W/nf * 0.29' pd='2*int((nf+1)/2) * (W/nf + 0.29)' ps='2*int((nf+2)/2) * (W/nf + 0.29)'
+ nrd='0.29 / W' nrs='0.29 / W' sa=0 sb=0 sd=0 mult=1 m=1
XM29 net25 net14 net14 GND sky130_fd_pr__nfet_01v8 L={L} W={W/2} nf=1 ad='int((nf+1)/2) * W/nf * 0.29'
+ as='int((nf+2)/2) * W/nf * 0.29' pd='2*int((nf+1)/2) * (W/nf + 0.29)' ps='2*int((nf+2)/2) * (W/nf + 0.29)'
+ nrd='0.29 / W' nrs='0.29 / W' sa=0 sb=0 sd=0 mult=1 m=1
XM70 net25 net16 GND GND sky130_fd_pr__nfet_01v8 L={L} W={W/2} nf=1 ad='int((nf+1)/2) * W/nf * 0.29'
+ as='int((nf+2)/2) * W/nf * 0.29' pd='2*int((nf+1)/2) * (W/nf + 0.29)' ps='2*int((nf+2)/2) * (W/nf + 0.29)'
+ nrd='0.29 / W' nrs='0.29 / W' sa=0 sb=0 sd=0 mult=1 m=1
XM71 GND Vbn net15 GND sky130_fd_pr__nfet_01v8 L={L} W={W/2} nf=1 ad='int((nf+1)/2) * W/nf * 0.29' as='int((nf+2)/2) * W/nf * 0.29'
+ pd='2*int((nf+1)/2) * (W/nf + 0.29)' ps='2*int((nf+2)/2) * (W/nf + 0.29)' nrd='0.29 / W' nrs='0.29 / W'
+ sa=0 sb=0 sd=0 mult=1 m=1
XM72 net16 net16 net25 GND sky130_fd_pr__nfet_01v8 L={L} W={W/2} nf=1 ad='int((nf+1)/2) * W/nf * 0.29'
+ as='int((nf+2)/2) * W/nf * 0.29' pd='2*int((nf+1)/2) * (W/nf + 0.29)' ps='2*int((nf+2)/2) * (W/nf + 0.29)'
+ nrd='0.29 / W' nrs='0.29 / W' sa=0 sb=0 sd=0 mult=1 m=1
XM73 net25 net16 net16 GND sky130_fd_pr__nfet_01v8 L={L} W={W/2} nf=1 ad='int((nf+1)/2) * W/nf * 0.29'
+ as='int((nf+2)/2) * W/nf * 0.29' pd='2*int((nf+1)/2) * (W/nf + 0.29)' ps='2*int((nf+2)/2) * (W/nf + 0.29)'
+ nrd='0.29 / W' nrs='0.29 / W' sa=0 sb=0 sd=0 mult=1 m=1
XM74 net16 net16 net25 GND sky130_fd_pr__nfet_01v8 L={L} W={W/2} nf=1 ad='int((nf+1)/2) * W/nf * 0.29'
+ as='int((nf+2)/2) * W/nf * 0.29' pd='2*int((nf+1)/2) * (W/nf + 0.29)' ps='2*int((nf+2)/2) * (W/nf + 0.29)'
+ nrd='0.29 / W' nrs='0.29 / W' sa=0 sb=0 sd=0 mult=1 m=1
XM77 net25 net16 net16 GND sky130_fd_pr__nfet_01v8 L={L} W={W/2} nf=1 ad='int((nf+1)/2) * W/nf * 0.29'
+ as='int((nf+2)/2) * W/nf * 0.29' pd='2*int((nf+1)/2) * (W/nf + 0.29)' ps='2*int((nf+2)/2) * (W/nf + 0.29)'
+ nrd='0.29 / W' nrs='0.29 / W' sa=0 sb=0 sd=0 mult=1 m=1
XM78 net14 net14 net25 GND sky130_fd_pr__nfet_01v8 L={L} W={W/2} nf=1 ad='int((nf+1)/2) * W/nf * 0.29'
+ as='int((nf+2)/2) * W/nf * 0.29' pd='2*int((nf+1)/2) * (W/nf + 0.29)' ps='2*int((nf+2)/2) * (W/nf + 0.29)'
+ nrd='0.29 / W' nrs='0.29 / W' sa=0 sb=0 sd=0 mult=1 m=1
XM80 GND net16 net25 GND sky130_fd_pr__nfet_01v8 L={L} W={W/2} nf=1 ad='int((nf+1)/2) * W/nf * 0.29'
+ as='int((nf+2)/2) * W/nf * 0.29' pd='2*int((nf+1)/2) * (W/nf + 0.29)' ps='2*int((nf+2)/2) * (W/nf + 0.29)'
+ nrd='0.29 / W' nrs='0.29 / W' sa=0 sb=0 sd=0 mult=1 m=1
XM84 net15 Vbn GND GND sky130_fd_pr__nfet_01v8 L={L} W={W/2} nf=1 ad='int((nf+1)/2) * W/nf * 0.29' as='int((nf+2)/2) * W/nf * 0.29'
+ pd='2*int((nf+1)/2) * (W/nf + 0.29)' ps='2*int((nf+2)/2) * (W/nf + 0.29)' nrd='0.29 / W' nrs='0.29 / W'
+ sa=0 sb=0 sd=0 mult=1 m=1
XM85 net15 GND GND GND sky130_fd_pr__nfet_01v8 L={L} W={W/2} nf=1 ad='int((nf+1)/2) * W/nf * 0.29' as='int((nf+2)/2) * W/nf * 0.29'
+ pd='2*int((nf+1)/2) * (W/nf + 0.29)' ps='2*int((nf+2)/2) * (W/nf + 0.29)' nrd='0.29 / W' nrs='0.29 / W'
+ sa=0 sb=0 sd=0 mult=1 m=1
XM152 GND GND net15 GND sky130_fd_pr__nfet_01v8 L={L} W={W/2} nf=1 ad='int((nf+1)/2) * W/nf * 0.29' as='int((nf+2)/2) * W/nf * 0.29'
+ pd='2*int((nf+1)/2) * (W/nf + 0.29)' ps='2*int((nf+2)/2) * (W/nf + 0.29)' nrd='0.29 / W' nrs='0.29 / W'
+ sa=0 sb=0 sd=0 mult=1 m=1
X1 GND Vbn b0out b0 mux
X2 GND Vbn b1out b1 mux
X3 GND Vbn net36 b2 mux
X4 GND Vbn net38 b3 mux
X5 GND Vbn net37 b4 mux
X6 GND Vbn net35 b5 mux
X8 GND Vbn b6out b6 mux
Vout1 VVout net33 0
.save i(vout1)
XM38 net27 net14 net26 GND sky130_fd_pr__nfet_01v8 L={L} W={W} nf=1 ad='int((nf+1)/2) * W/nf * 0.29'
+ as='int((nf+2)/2) * W/nf * 0.29' pd='2*int((nf+1)/2) * (W/nf + 0.29)' ps='2*int((nf+2)/2) * (W/nf + 0.29)'
+ nrd='0.29 / W' nrs='0.29 / W' sa=0 sb=0 sd=0 mult=1 m=1
XM39 net26 net14 net27 GND sky130_fd_pr__nfet_01v8 L={L} W={W} nf=1 ad='int((nf+1)/2) * W/nf * 0.29'
+ as='int((nf+2)/2) * W/nf * 0.29' pd='2*int((nf+1)/2) * (W/nf + 0.29)' ps='2*int((nf+2)/2) * (W/nf + 0.29)'
+ nrd='0.29 / W' nrs='0.29 / W' sa=0 sb=0 sd=0 mult=1 m=1
XM40 net27 net14 net28 GND sky130_fd_pr__nfet_01v8 L={L} W={W} nf=1 ad='int((nf+1)/2) * W/nf * 0.29'
+ as='int((nf+2)/2) * W/nf * 0.29' pd='2*int((nf+1)/2) * (W/nf + 0.29)' ps='2*int((nf+2)/2) * (W/nf + 0.29)'
+ nrd='0.29 / W' nrs='0.29 / W' sa=0 sb=0 sd=0 mult=1 m=1
XM41 net28 net14 net27 GND sky130_fd_pr__nfet_01v8 L={L} W={W} nf=1 ad='int((nf+1)/2) * W/nf * 0.29'
+ as='int((nf+2)/2) * W/nf * 0.29' pd='2*int((nf+1)/2) * (W/nf + 0.29)' ps='2*int((nf+2)/2) * (W/nf + 0.29)'
+ nrd='0.29 / W' nrs='0.29 / W' sa=0 sb=0 sd=0 mult=1 m=1
XM42 GND b0out net27 GND sky130_fd_pr__nfet_01v8 L={L} W={W} nf=1 ad='int((nf+1)/2) * W/nf * 0.29' as='int((nf+2)/2) * W/nf * 0.29'
+ pd='2*int((nf+1)/2) * (W/nf + 0.29)' ps='2*int((nf+2)/2) * (W/nf + 0.29)' nrd='0.29 / W' nrs='0.29 / W'
+ sa=0 sb=0 sd=0 mult=1 m=1
XM43 net26 b1out GND GND sky130_fd_pr__nfet_01v8 L={L} W={W} nf=1 ad='int((nf+1)/2) * W/nf * 0.29' as='int((nf+2)/2) * W/nf * 0.29'
+ pd='2*int((nf+1)/2) * (W/nf + 0.29)' ps='2*int((nf+2)/2) * (W/nf + 0.29)' nrd='0.29 / W' nrs='0.29 / W'
+ sa=0 sb=0 sd=0 mult=1 m=1
XM44 GND net35 net29 GND sky130_fd_pr__nfet_01v8 L={L} W={W} nf=1 ad='int((nf+1)/2) * W/nf * 0.29' as='int((nf+2)/2) * W/nf * 0.29'
+ pd='2*int((nf+1)/2) * (W/nf + 0.29)' ps='2*int((nf+2)/2) * (W/nf + 0.29)' nrd='0.29 / W' nrs='0.29 / W'
+ sa=0 sb=0 sd=0 mult=1 m=1
XM45 net26 net14 net30 GND sky130_fd_pr__nfet_01v8 L={L} W={W} nf=1 ad='int((nf+1)/2) * W/nf * 0.29'
+ as='int((nf+2)/2) * W/nf * 0.29' pd='2*int((nf+1)/2) * (W/nf + 0.29)' ps='2*int((nf+2)/2) * (W/nf + 0.29)'
+ nrd='0.29 / W' nrs='0.29 / W' sa=0 sb=0 sd=0 mult=1 m=1
XM46 net30 net14 net26 GND sky130_fd_pr__nfet_01v8 L={L} W={W} nf=1 ad='int((nf+1)/2) * W/nf * 0.29'
+ as='int((nf+2)/2) * W/nf * 0.29' pd='2*int((nf+1)/2) * (W/nf + 0.29)' ps='2*int((nf+2)/2) * (W/nf + 0.29)'
+ nrd='0.29 / W' nrs='0.29 / W' sa=0 sb=0 sd=0 mult=1 m=1
XM96 net26 net14 net28 GND sky130_fd_pr__nfet_01v8 L={L} W={W} nf=1 ad='int((nf+1)/2) * W/nf * 0.29'
+ as='int((nf+2)/2) * W/nf * 0.29' pd='2*int((nf+1)/2) * (W/nf + 0.29)' ps='2*int((nf+2)/2) * (W/nf + 0.29)'
+ nrd='0.29 / W' nrs='0.29 / W' sa=0 sb=0 sd=0 mult=1 m=1
XM97 net28 net14 net30 GND sky130_fd_pr__nfet_01v8 L={L} W={W} nf=1 ad='int((nf+1)/2) * W/nf * 0.29'
+ as='int((nf+2)/2) * W/nf * 0.29' pd='2*int((nf+1)/2) * (W/nf + 0.29)' ps='2*int((nf+2)/2) * (W/nf + 0.29)'
+ nrd='0.29 / W' nrs='0.29 / W' sa=0 sb=0 sd=0 mult=1 m=1
XM98 net30 net14 net31 GND sky130_fd_pr__nfet_01v8 L={L} W={W} nf=1 ad='int((nf+1)/2) * W/nf * 0.29'
+ as='int((nf+2)/2) * W/nf * 0.29' pd='2*int((nf+1)/2) * (W/nf + 0.29)' ps='2*int((nf+2)/2) * (W/nf + 0.29)'
+ nrd='0.29 / W' nrs='0.29 / W' sa=0 sb=0 sd=0 mult=1 m=1
XM99 net31 net14 net30 GND sky130_fd_pr__nfet_01v8 L={L} W={W} nf=1 ad='int((nf+1)/2) * W/nf * 0.29'
+ as='int((nf+2)/2) * W/nf * 0.29' pd='2*int((nf+1)/2) * (W/nf + 0.29)' ps='2*int((nf+2)/2) * (W/nf + 0.29)'
+ nrd='0.29 / W' nrs='0.29 / W' sa=0 sb=0 sd=0 mult=1 m=1
XM100 GND net36 net30 GND sky130_fd_pr__nfet_01v8 L={L} W={W} nf=1 ad='int((nf+1)/2) * W/nf * 0.29' as='int((nf+2)/2) * W/nf * 0.29'
+ pd='2*int((nf+1)/2) * (W/nf + 0.29)' ps='2*int((nf+2)/2) * (W/nf + 0.29)' nrd='0.29 / W' nrs='0.29 / W'
+ sa=0 sb=0 sd=0 mult=1 m=1
XM101 net32 net14 net29 GND sky130_fd_pr__nfet_01v8 L={L} W={W} nf=1 ad='int((nf+1)/2) * W/nf * 0.29'
+ as='int((nf+2)/2) * W/nf * 0.29' pd='2*int((nf+1)/2) * (W/nf + 0.29)' ps='2*int((nf+2)/2) * (W/nf + 0.29)'
+ nrd='0.29 / W' nrs='0.29 / W' sa=0 sb=0 sd=0 mult=1 m=1
XM102 net29 net14 net32 GND sky130_fd_pr__nfet_01v8 L={L} W={W} nf=1 ad='int((nf+1)/2) * W/nf * 0.29'
+ as='int((nf+2)/2) * W/nf * 0.29' pd='2*int((nf+1)/2) * (W/nf + 0.29)' ps='2*int((nf+2)/2) * (W/nf + 0.29)'
+ nrd='0.29 / W' nrs='0.29 / W' sa=0 sb=0 sd=0 mult=1 m=1
XM103 net28 net14 net29 GND sky130_fd_pr__nfet_01v8 L={L} W={W} nf=1 ad='int((nf+1)/2) * W/nf * 0.29'
+ as='int((nf+2)/2) * W/nf * 0.29' pd='2*int((nf+1)/2) * (W/nf + 0.29)' ps='2*int((nf+2)/2) * (W/nf + 0.29)'
+ nrd='0.29 / W' nrs='0.29 / W' sa=0 sb=0 sd=0 mult=1 m=1
XM104 net32 net14 net28 GND sky130_fd_pr__nfet_01v8 L={L} W={W} nf=1 ad='int((nf+1)/2) * W/nf * 0.29'
+ as='int((nf+2)/2) * W/nf * 0.29' pd='2*int((nf+1)/2) * (W/nf + 0.29)' ps='2*int((nf+2)/2) * (W/nf + 0.29)'
+ nrd='0.29 / W' nrs='0.29 / W' sa=0 sb=0 sd=0 mult=1 m=1
XM105 net31 net14 net32 GND sky130_fd_pr__nfet_01v8 L={L} W={W} nf=1 ad='int((nf+1)/2) * W/nf * 0.29'
+ as='int((nf+2)/2) * W/nf * 0.29' pd='2*int((nf+1)/2) * (W/nf + 0.29)' ps='2*int((nf+2)/2) * (W/nf + 0.29)'
+ nrd='0.29 / W' nrs='0.29 / W' sa=0 sb=0 sd=0 mult=1 m=1
XM106 net32 net14 net31 GND sky130_fd_pr__nfet_01v8 L={L} W={W} nf=1 ad='int((nf+1)/2) * W/nf * 0.29'
+ as='int((nf+2)/2) * W/nf * 0.29' pd='2*int((nf+1)/2) * (W/nf + 0.29)' ps='2*int((nf+2)/2) * (W/nf + 0.29)'
+ nrd='0.29 / W' nrs='0.29 / W' sa=0 sb=0 sd=0 mult=1 m=1
XM107 net32 net37 GND GND sky130_fd_pr__nfet_01v8 L={L} W={W} nf=1 ad='int((nf+1)/2) * W/nf * 0.29' as='int((nf+2)/2) * W/nf * 0.29'
+ pd='2*int((nf+1)/2) * (W/nf + 0.29)' ps='2*int((nf+2)/2) * (W/nf + 0.29)' nrd='0.29 / W' nrs='0.29 / W'
+ sa=0 sb=0 sd=0 mult=1 m=1
XM108 net33 net14 net34 GND sky130_fd_pr__nfet_01v8 L={L} W={W} nf=1 ad='int((nf+1)/2) * W/nf * 0.29'
+ as='int((nf+2)/2) * W/nf * 0.29' pd='2*int((nf+1)/2) * (W/nf + 0.29)' ps='2*int((nf+2)/2) * (W/nf + 0.29)'
+ nrd='0.29 / W' nrs='0.29 / W' sa=0 sb=0 sd=0 mult=1 m=1
XM109 net34 net14 net33 GND sky130_fd_pr__nfet_01v8 L={L} W={W} nf=1 ad='int((nf+1)/2) * W/nf * 0.29'
+ as='int((nf+2)/2) * W/nf * 0.29' pd='2*int((nf+1)/2) * (W/nf + 0.29)' ps='2*int((nf+2)/2) * (W/nf + 0.29)'
+ nrd='0.29 / W' nrs='0.29 / W' sa=0 sb=0 sd=0 mult=1 m=1
XM110 net29 net14 net34 GND sky130_fd_pr__nfet_01v8 L={L} W={W} nf=1 ad='int((nf+1)/2) * W/nf * 0.29'
+ as='int((nf+2)/2) * W/nf * 0.29' pd='2*int((nf+1)/2) * (W/nf + 0.29)' ps='2*int((nf+2)/2) * (W/nf + 0.29)'
+ nrd='0.29 / W' nrs='0.29 / W' sa=0 sb=0 sd=0 mult=1 m=1
XM111 net34 net14 net29 GND sky130_fd_pr__nfet_01v8 L={L} W={W} nf=1 ad='int((nf+1)/2) * W/nf * 0.29'
+ as='int((nf+2)/2) * W/nf * 0.29' pd='2*int((nf+1)/2) * (W/nf + 0.29)' ps='2*int((nf+2)/2) * (W/nf + 0.29)'
+ nrd='0.29 / W' nrs='0.29 / W' sa=0 sb=0 sd=0 mult=1 m=1
XM112 net34 b6out GND GND sky130_fd_pr__nfet_01v8 L={L} W={W} nf=1 ad='int((nf+1)/2) * W/nf * 0.29' as='int((nf+2)/2) * W/nf * 0.29'
+ pd='2*int((nf+1)/2) * (W/nf + 0.29)' ps='2*int((nf+2)/2) * (W/nf + 0.29)' nrd='0.29 / W' nrs='0.29 / W'
+ sa=0 sb=0 sd=0 mult=1 m=1
XM113 GND net38 net31 GND sky130_fd_pr__nfet_01v8 L={L} W={W} nf=1 ad='int((nf+1)/2) * W/nf * 0.29' as='int((nf+2)/2) * W/nf * 0.29'
+ pd='2*int((nf+1)/2) * (W/nf + 0.29)' ps='2*int((nf+2)/2) * (W/nf + 0.29)' nrd='0.29 / W' nrs='0.29 / W'
+ sa=0 sb=0 sd=0 mult=1 m=1
XM114 net28 net14 net31 GND sky130_fd_pr__nfet_01v8 L={L} W={W} nf=1 ad='int((nf+1)/2) * W/nf * 0.29'
+ as='int((nf+2)/2) * W/nf * 0.29' pd='2*int((nf+1)/2) * (W/nf + 0.29)' ps='2*int((nf+2)/2) * (W/nf + 0.29)'
+ nrd='0.29 / W' nrs='0.29 / W' sa=0 sb=0 sd=0 mult=1 m=1
XM115 VDD net28 net28 VDD sky130_fd_pr__pfet_01v8 L={L} W={W} nf=1 ad='int((nf+1)/2) * W/nf * 0.29' as='int((nf+2)/2) * W/nf * 0.29'
+ pd='2*int((nf+1)/2) * (W/nf + 0.29)' ps='2*int((nf+2)/2) * (W/nf + 0.29)' nrd='0.29 / W' nrs='0.29 / W'
+ sa=0 sb=0 sd=0 mult=1 m=1
Vout3 net39 GND 1.8
V7 b0 GND 1.8
V8 b1 GND 1.8
V9 b2 GND 1.8
V10 b3 GND 1.8
V11 b4 GND 1.8
V12 b5 GND 1.8
V13 b6 GND 1.8
VDD14 VDD GND 1.8
**** begin user architecture code

.param W=24
.param L=1
.dc Vout3 0 1.8 0.01
.save v(Vout3) i(Vout) v(VVout)


.option wnflag=1
.param MC_SWITCH=0.0
.lib ~/skywater/skywater-pdk/libraries/sky130_fd_pr_ngspice/latest/models/sky130.lib.spice tt

**** end user architecture code
**.ends

* expanding   symbol:  /home/madvlsi/Documents/current-output-dac-vlsi/schematics/mux.sym # of
*+ pins=4
** sym_path: /home/madvlsi/Documents/current-output-dac-vlsi/schematics/mux.sym
** sch_path: /home/madvlsi/Documents/current-output-dac-vlsi/schematics/mux.sch
.subckt mux A B Y S
*.ipin S
*.ipin A
*.opin Y
*.ipin B
XM1 net1 S GND GND sky130_fd_pr__nfet_01v8 L=0.15 W=1 nf=1 ad='int((nf+1)/2) * W/nf * 0.29' as='int((nf+2)/2) * W/nf * 0.29'
+ pd='2*int((nf+1)/2) * (W/nf + 0.29)' ps='2*int((nf+2)/2) * (W/nf + 0.29)' nrd='0.29 / W' nrs='0.29 / W'
+ sa=0 sb=0 sd=0 mult=1 m=1
XM2 net1 S VDD VDD sky130_fd_pr__pfet_01v8 L=0.15 W=1 nf=1 ad='int((nf+1)/2) * W/nf * 0.29' as='int((nf+2)/2) * W/nf * 0.29'
+ pd='2*int((nf+1)/2) * (W/nf + 0.29)' ps='2*int((nf+2)/2) * (W/nf + 0.29)' nrd='0.29 / W' nrs='0.29 / W'
+ sa=0 sb=0 sd=0 mult=1 m=1
XM3 Y S B GND sky130_fd_pr__nfet_01v8 L=0.15 W=1 nf=1 ad='int((nf+1)/2) * W/nf * 0.29' as='int((nf+2)/2) * W/nf * 0.29'
+ pd='2*int((nf+1)/2) * (W/nf + 0.29)' ps='2*int((nf+2)/2) * (W/nf + 0.29)' nrd='0.29 / W' nrs='0.29 / W'
+ sa=0 sb=0 sd=0 mult=1 m=1
XM4 A net1 Y GND sky130_fd_pr__nfet_01v8 L=0.15 W=1 nf=1 ad='int((nf+1)/2) * W/nf * 0.29' as='int((nf+2)/2) * W/nf * 0.29'
+ pd='2*int((nf+1)/2) * (W/nf + 0.29)' ps='2*int((nf+2)/2) * (W/nf + 0.29)' nrd='0.29 / W' nrs='0.29 / W'
+ sa=0 sb=0 sd=0 mult=1 m=1
.ends

.GLOBAL VDD
.GLOBAL GND
.end
